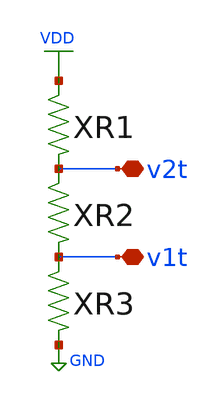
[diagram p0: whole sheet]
** sch_path: xschem/vdiv.sch
**.subckt vdiv v2t v1t
*.iopin v2t
*.iopin v1t
XR1 v2t VDD res100k
XR2 v1t v2t res100k
XR3 GND v1t res100k
**.ends

* expanding   symbol:  res100k.sym # of pins=2
** sym_path: xschem/res100k.sym
** sch_path: xschem/res100k.sch
.subckt res100k bot top
*.iopin top
*.iopin bot
XR1 net1 top GND sky130_fd_pr__res_xhigh_po W=0.35 L=3.5 mult=1 m=1
XR2 net2 net1 GND sky130_fd_pr__res_xhigh_po W=0.35 L=3.5 mult=1 m=1
XR3 net3 net2 GND sky130_fd_pr__res_xhigh_po W=0.35 L=3.5 mult=1 m=1
XR4 net4 net3 GND sky130_fd_pr__res_xhigh_po W=0.35 L=3.5 mult=1 m=1
XR5 bot net4 GND sky130_fd_pr__res_xhigh_po W=0.35 L=3.5 mult=1 m=1
.ends

.GLOBAL VDD
.GLOBAL GND
.end
